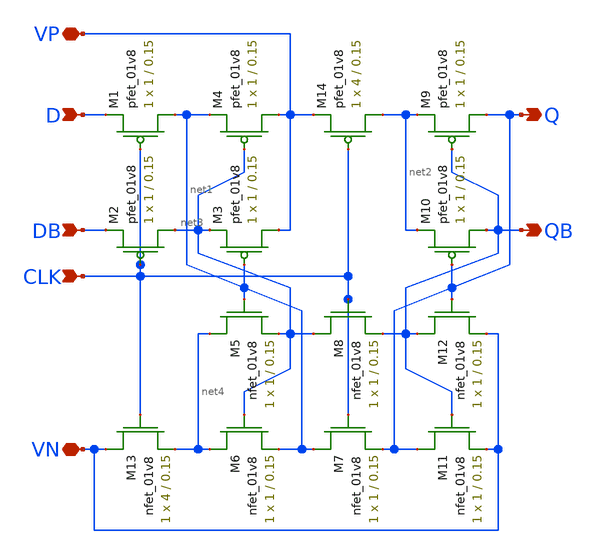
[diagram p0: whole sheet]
** sch_path: MP2/xschem/final/csrl_dff3_lds (copy).sch
**.subckt csrl_dff3_lds (copy) D DB CLK Q QB VP VN
*.ipin D
*.ipin DB
*.ipin CLK
*.opin Q
*.opin QB
*.iopin VP
*.iopin VN
XM1 net1 CLK D VDD sky130_fd_pr__pfet_01v8 L=0.15 W=1 nf=1 ad='int((nf+1)/2) * W/nf * 0.29' as='int((nf+2)/2) * W/nf * 0.29'
+ pd='2*int((nf+1)/2) * (W/nf + 0.29)' ps='2*int((nf+2)/2) * (W/nf + 0.29)' nrd='0.29 / W' nrs='0.29 / W'
+ sa=0 sb=0 sd=0 mult=1 m=1
XM2 net3 CLK DB VDD sky130_fd_pr__pfet_01v8 L=0.15 W=1 nf=1 ad='int((nf+1)/2) * W/nf * 0.29' as='int((nf+2)/2) * W/nf * 0.29'
+ pd='2*int((nf+1)/2) * (W/nf + 0.29)' ps='2*int((nf+2)/2) * (W/nf + 0.29)' nrd='0.29 / W' nrs='0.29 / W'
+ sa=0 sb=0 sd=0 mult=1 m=1
XM3 VP net1 net3 VDD sky130_fd_pr__pfet_01v8 L=0.15 W=1 nf=1 ad='int((nf+1)/2) * W/nf * 0.29' as='int((nf+2)/2) * W/nf * 0.29'
+ pd='2*int((nf+1)/2) * (W/nf + 0.29)' ps='2*int((nf+2)/2) * (W/nf + 0.29)' nrd='0.29 / W' nrs='0.29 / W'
+ sa=0 sb=0 sd=0 mult=1 m=1
XM4 VP net3 net1 VDD sky130_fd_pr__pfet_01v8 L=0.15 W=1 nf=1 ad='int((nf+1)/2) * W/nf * 0.29' as='int((nf+2)/2) * W/nf * 0.29'
+ pd='2*int((nf+1)/2) * (W/nf + 0.29)' ps='2*int((nf+2)/2) * (W/nf + 0.29)' nrd='0.29 / W' nrs='0.29 / W'
+ sa=0 sb=0 sd=0 mult=1 m=1
XM5 net4 net1 net3 GND sky130_fd_pr__nfet_01v8 L=0.15 W=1 nf=1 ad='int((nf+1)/2) * W/nf * 0.29' as='int((nf+2)/2) * W/nf * 0.29'
+ pd='2*int((nf+1)/2) * (W/nf + 0.29)' ps='2*int((nf+2)/2) * (W/nf + 0.29)' nrd='0.29 / W' nrs='0.29 / W'
+ sa=0 sb=0 sd=0 mult=1 m=1
XM6 net4 net3 net1 GND sky130_fd_pr__nfet_01v8 L=0.15 W=1 nf=1 ad='int((nf+1)/2) * W/nf * 0.29' as='int((nf+2)/2) * W/nf * 0.29'
+ pd='2*int((nf+1)/2) * (W/nf + 0.29)' ps='2*int((nf+2)/2) * (W/nf + 0.29)' nrd='0.29 / W' nrs='0.29 / W'
+ sa=0 sb=0 sd=0 mult=1 m=1
XM7 net1 CLK Q GND sky130_fd_pr__nfet_01v8 L=0.15 W=1 nf=1 ad='int((nf+1)/2) * W/nf * 0.29' as='int((nf+2)/2) * W/nf * 0.29'
+ pd='2*int((nf+1)/2) * (W/nf + 0.29)' ps='2*int((nf+2)/2) * (W/nf + 0.29)' nrd='0.29 / W' nrs='0.29 / W'
+ sa=0 sb=0 sd=0 mult=1 m=1
XM8 net3 CLK QB GND sky130_fd_pr__nfet_01v8 L=0.15 W=1 nf=1 ad='int((nf+1)/2) * W/nf * 0.29' as='int((nf+2)/2) * W/nf * 0.29'
+ pd='2*int((nf+1)/2) * (W/nf + 0.29)' ps='2*int((nf+2)/2) * (W/nf + 0.29)' nrd='0.29 / W' nrs='0.29 / W'
+ sa=0 sb=0 sd=0 mult=1 m=1
XM9 Q QB net2 VDD sky130_fd_pr__pfet_01v8 L=0.15 W=1 nf=1 ad='int((nf+1)/2) * W/nf * 0.29' as='int((nf+2)/2) * W/nf * 0.29'
+ pd='2*int((nf+1)/2) * (W/nf + 0.29)' ps='2*int((nf+2)/2) * (W/nf + 0.29)' nrd='0.29 / W' nrs='0.29 / W'
+ sa=0 sb=0 sd=0 mult=1 m=1
XM10 QB Q net2 VDD sky130_fd_pr__pfet_01v8 L=0.15 W=1 nf=1 ad='int((nf+1)/2) * W/nf * 0.29' as='int((nf+2)/2) * W/nf * 0.29'
+ pd='2*int((nf+1)/2) * (W/nf + 0.29)' ps='2*int((nf+2)/2) * (W/nf + 0.29)' nrd='0.29 / W' nrs='0.29 / W'
+ sa=0 sb=0 sd=0 mult=1 m=1
XM11 Q QB VN GND sky130_fd_pr__nfet_01v8 L=0.15 W=1 nf=1 ad='int((nf+1)/2) * W/nf * 0.29' as='int((nf+2)/2) * W/nf * 0.29'
+ pd='2*int((nf+1)/2) * (W/nf + 0.29)' ps='2*int((nf+2)/2) * (W/nf + 0.29)' nrd='0.29 / W' nrs='0.29 / W'
+ sa=0 sb=0 sd=0 mult=1 m=1
XM12 QB Q VN GND sky130_fd_pr__nfet_01v8 L=0.15 W=1 nf=1 ad='int((nf+1)/2) * W/nf * 0.29' as='int((nf+2)/2) * W/nf * 0.29'
+ pd='2*int((nf+1)/2) * (W/nf + 0.29)' ps='2*int((nf+2)/2) * (W/nf + 0.29)' nrd='0.29 / W' nrs='0.29 / W'
+ sa=0 sb=0 sd=0 mult=1 m=1
XM13 VN CLK net4 GND sky130_fd_pr__nfet_01v8 L=0.15 W=4 nf=1 ad='int((nf+1)/2) * W/nf * 0.29' as='int((nf+2)/2) * W/nf * 0.29'
+ pd='2*int((nf+1)/2) * (W/nf + 0.29)' ps='2*int((nf+2)/2) * (W/nf + 0.29)' nrd='0.29 / W' nrs='0.29 / W'
+ sa=0 sb=0 sd=0 mult=1 m=1
XM14 net2 CLK VP VDD sky130_fd_pr__pfet_01v8 L=0.15 W=4 nf=1 ad='int((nf+1)/2) * W/nf * 0.29' as='int((nf+2)/2) * W/nf * 0.29'
+ pd='2*int((nf+1)/2) * (W/nf + 0.29)' ps='2*int((nf+2)/2) * (W/nf + 0.29)' nrd='0.29 / W' nrs='0.29 / W'
+ sa=0 sb=0 sd=0 mult=1 m=1
**.ends
.end
